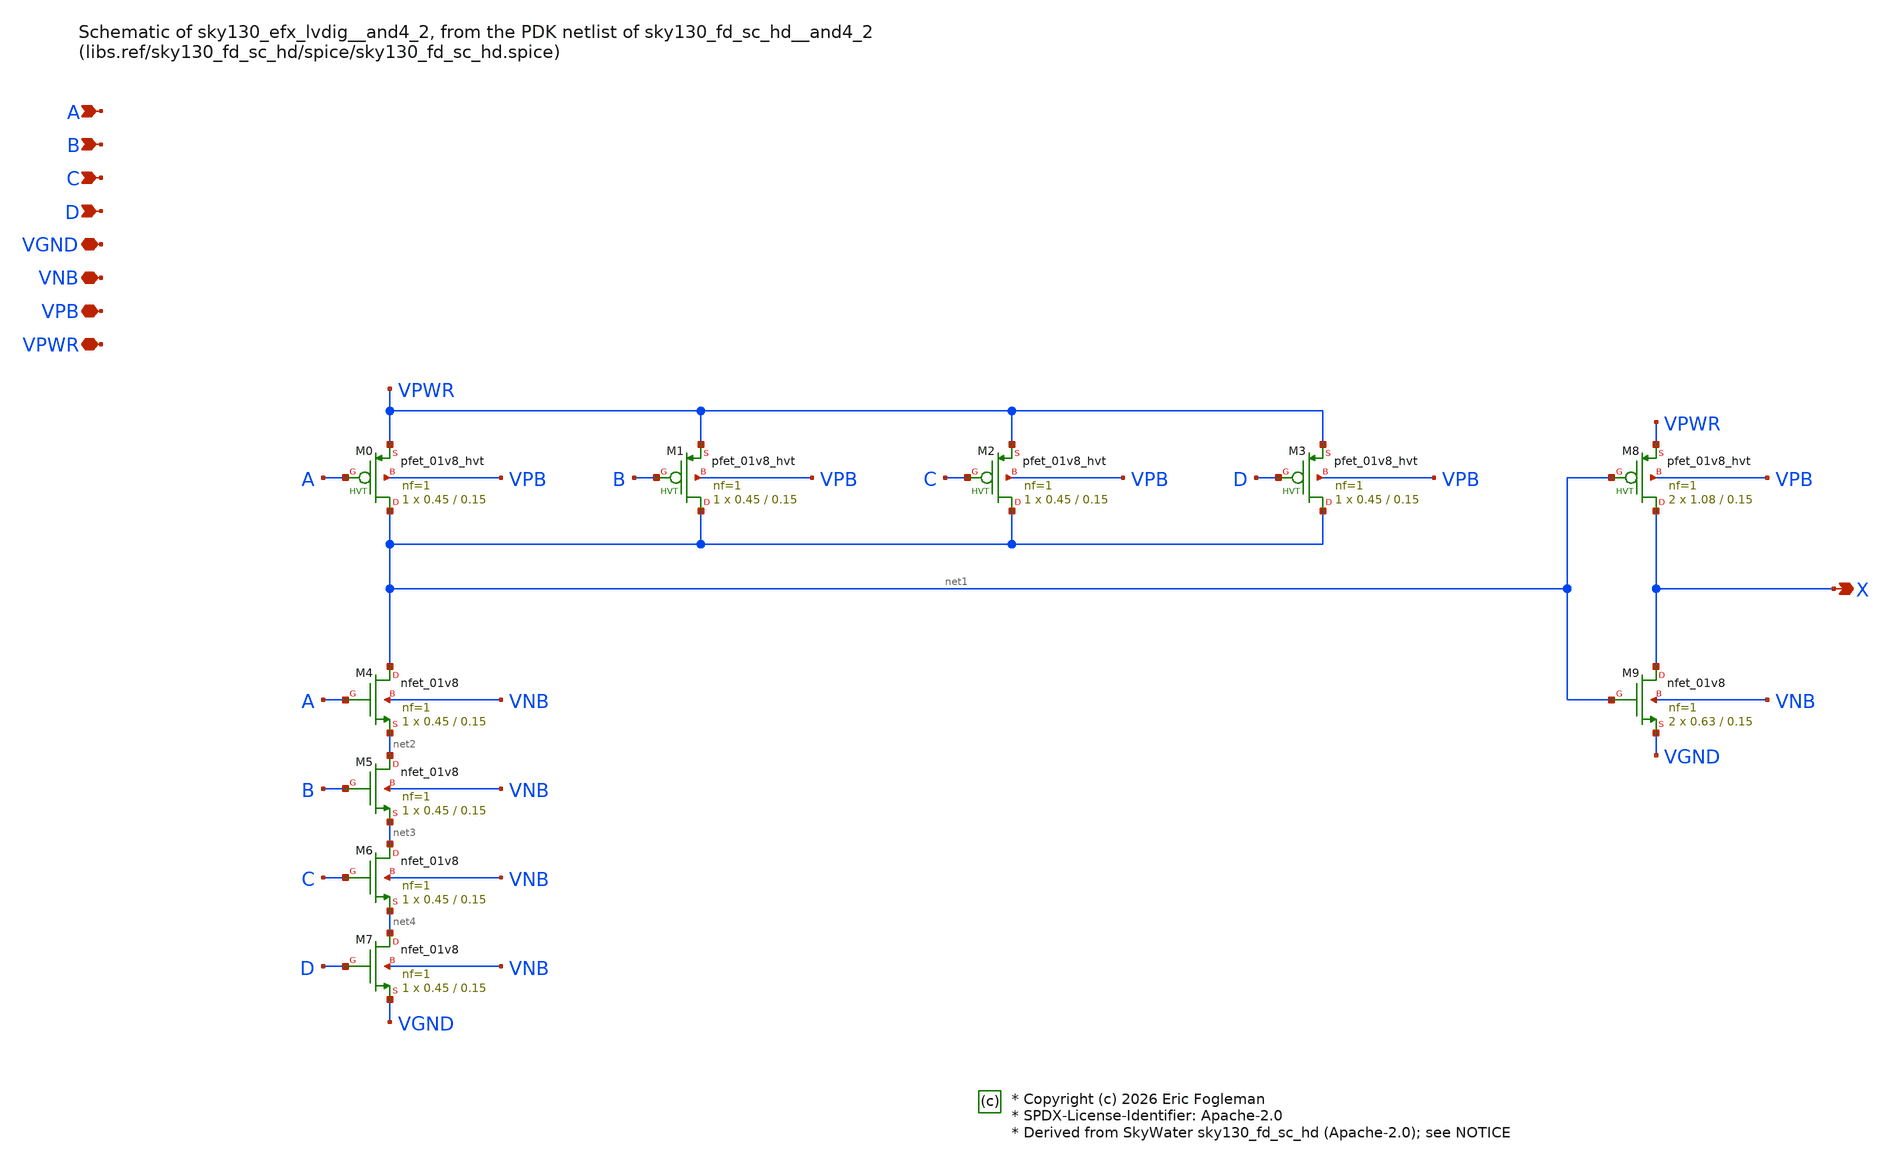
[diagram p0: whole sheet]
** sch_path: xschem/sky130_efx_lvdig__and4_2.sch

* Copyright (c) 2026 Eric Fogleman
* SPDX-License-Identifier: Apache-2.0
* Derived from SkyWater sky130_fd_sc_hd (Apache-2.0); see NOTICE

**.subckt sky130_efx_lvdig__and4_2 X A B C D VGND VNB VPB VPWR
*.opin X
*.ipin A
*.ipin B
*.ipin C
*.ipin D
*.iopin VGND
*.iopin VNB
*.iopin VPB
*.iopin VPWR
XM0 net1 A VPWR VPB sky130_fd_pr__pfet_01v8_hvt L=0.15 W=0.45 nf=1 ad='int((1 + 1)/2) * 0.45 / 1 * 0.29'
+ as='int((1 + 2)/2) * 0.45 / 1 * 0.29' pd='2*int((1 + 1)/2) * (0.45 / 1 + 0.29)' ps='2*int((1 + 2)/2) * (0.45 / 1 + 0.29)'
+ nrd='0.29 / 0.45 ' nrs='0.29 / 0.45 ' sa=0 sb=0 sd=0 mult=1 m=1
XM1 net1 B VPWR VPB sky130_fd_pr__pfet_01v8_hvt L=0.15 W=0.45 nf=1 ad='int((1 + 1)/2) * 0.45 / 1 * 0.29'
+ as='int((1 + 2)/2) * 0.45 / 1 * 0.29' pd='2*int((1 + 1)/2) * (0.45 / 1 + 0.29)' ps='2*int((1 + 2)/2) * (0.45 / 1 + 0.29)'
+ nrd='0.29 / 0.45 ' nrs='0.29 / 0.45 ' sa=0 sb=0 sd=0 mult=1 m=1
XM2 net1 C VPWR VPB sky130_fd_pr__pfet_01v8_hvt L=0.15 W=0.45 nf=1 ad='int((1 + 1)/2) * 0.45 / 1 * 0.29'
+ as='int((1 + 2)/2) * 0.45 / 1 * 0.29' pd='2*int((1 + 1)/2) * (0.45 / 1 + 0.29)' ps='2*int((1 + 2)/2) * (0.45 / 1 + 0.29)'
+ nrd='0.29 / 0.45 ' nrs='0.29 / 0.45 ' sa=0 sb=0 sd=0 mult=1 m=1
XM3 net1 D VPWR VPB sky130_fd_pr__pfet_01v8_hvt L=0.15 W=0.45 nf=1 ad='int((1 + 1)/2) * 0.45 / 1 * 0.29'
+ as='int((1 + 2)/2) * 0.45 / 1 * 0.29' pd='2*int((1 + 1)/2) * (0.45 / 1 + 0.29)' ps='2*int((1 + 2)/2) * (0.45 / 1 + 0.29)'
+ nrd='0.29 / 0.45 ' nrs='0.29 / 0.45 ' sa=0 sb=0 sd=0 mult=1 m=1
XM4 net1 A net2 VNB sky130_fd_pr__nfet_01v8 L=0.15 W=0.45 nf=1 ad='int((1 + 1)/2) * 0.45 / 1 * 0.29'
+ as='int((1 + 2)/2) * 0.45 / 1 * 0.29' pd='2*int((1 + 1)/2) * (0.45 / 1 + 0.29)' ps='2*int((1 + 2)/2) * (0.45 / 1 + 0.29)'
+ nrd='0.29 / 0.45 ' nrs='0.29 / 0.45 ' sa=0 sb=0 sd=0 mult=1 m=1
XM5 net2 B net3 VNB sky130_fd_pr__nfet_01v8 L=0.15 W=0.45 nf=1 ad='int((1 + 1)/2) * 0.45 / 1 * 0.29'
+ as='int((1 + 2)/2) * 0.45 / 1 * 0.29' pd='2*int((1 + 1)/2) * (0.45 / 1 + 0.29)' ps='2*int((1 + 2)/2) * (0.45 / 1 + 0.29)'
+ nrd='0.29 / 0.45 ' nrs='0.29 / 0.45 ' sa=0 sb=0 sd=0 mult=1 m=1
XM6 net3 C net4 VNB sky130_fd_pr__nfet_01v8 L=0.15 W=0.45 nf=1 ad='int((1 + 1)/2) * 0.45 / 1 * 0.29'
+ as='int((1 + 2)/2) * 0.45 / 1 * 0.29' pd='2*int((1 + 1)/2) * (0.45 / 1 + 0.29)' ps='2*int((1 + 2)/2) * (0.45 / 1 + 0.29)'
+ nrd='0.29 / 0.45 ' nrs='0.29 / 0.45 ' sa=0 sb=0 sd=0 mult=1 m=1
XM7 net4 D VGND VNB sky130_fd_pr__nfet_01v8 L=0.15 W=0.45 nf=1 ad='int((1 + 1)/2) * 0.45 / 1 * 0.29'
+ as='int((1 + 2)/2) * 0.45 / 1 * 0.29' pd='2*int((1 + 1)/2) * (0.45 / 1 + 0.29)' ps='2*int((1 + 2)/2) * (0.45 / 1 + 0.29)'
+ nrd='0.29 / 0.45 ' nrs='0.29 / 0.45 ' sa=0 sb=0 sd=0 mult=1 m=1
XM8 X net1 VPWR VPB sky130_fd_pr__pfet_01v8_hvt L=0.15 W=1.08 nf=1 ad='int((1 + 1)/2) * 1.08 / 1 * 0.29'
+ as='int((1 + 2)/2) * 1.08 / 1 * 0.29' pd='2*int((1 + 1)/2) * (1.08 / 1 + 0.29)' ps='2*int((1 + 2)/2) * (1.08 / 1 + 0.29)'
+ nrd='0.29 / 1.08 ' nrs='0.29 / 1.08 ' sa=0 sb=0 sd=0 mult=2 m=2
XM9 X net1 VGND VNB sky130_fd_pr__nfet_01v8 L=0.15 W=0.63 nf=1 ad='int((1 + 1)/2) * 0.63 / 1 * 0.29'
+ as='int((1 + 2)/2) * 0.63 / 1 * 0.29' pd='2*int((1 + 1)/2) * (0.63 / 1 + 0.29)' ps='2*int((1 + 2)/2) * (0.63 / 1 + 0.29)'
+ nrd='0.29 / 0.63 ' nrs='0.29 / 0.63 ' sa=0 sb=0 sd=0 mult=2 m=2
**.ends
.end
